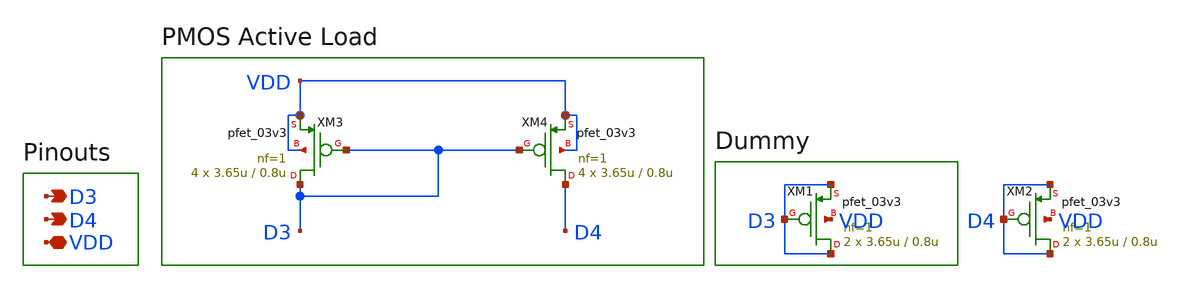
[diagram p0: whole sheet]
** sch_path: designs/libs/core_ota/active_load/active_load.sch
**.subckt active_load VDD D3 D4
*.iopin VDD
*.opin D3
*.opin D4
XM3 D3 D3 VDD VDD pfet_03v3 L=0.8u W=3.65u nf=1 ad='int((nf+1)/2) * W/nf * 0.18u' as='int((nf+2)/2) * W/nf * 0.18u'
+ pd='2*int((nf+1)/2) * (W/nf + 0.18u)' ps='2*int((nf+2)/2) * (W/nf + 0.18u)' nrd='0.18u / W' nrs='0.18u / W'
+ sa=0 sb=0 sd=0 m=4
XM4 D4 D3 VDD VDD pfet_03v3 L=0.8u W=3.65u nf=1 ad='int((nf+1)/2) * W/nf * 0.18u' as='int((nf+2)/2) * W/nf * 0.18u'
+ pd='2*int((nf+1)/2) * (W/nf + 0.18u)' ps='2*int((nf+2)/2) * (W/nf + 0.18u)' nrd='0.18u / W' nrs='0.18u / W'
+ sa=0 sb=0 sd=0 m=4
XM1 D3 D3 D3 VDD pfet_03v3 L=0.8u W=3.65u nf=1 ad='int((nf+1)/2) * W/nf * 0.18u' as='int((nf+2)/2) * W/nf * 0.18u'
+ pd='2*int((nf+1)/2) * (W/nf + 0.18u)' ps='2*int((nf+2)/2) * (W/nf + 0.18u)' nrd='0.18u / W' nrs='0.18u / W'
+ sa=0 sb=0 sd=0 m=2
XM2 D4 D4 D4 VDD pfet_03v3 L=0.8u W=3.65u nf=1 ad='int((nf+1)/2) * W/nf * 0.18u' as='int((nf+2)/2) * W/nf * 0.18u'
+ pd='2*int((nf+1)/2) * (W/nf + 0.18u)' ps='2*int((nf+2)/2) * (W/nf + 0.18u)' nrd='0.18u / W' nrs='0.18u / W'
+ sa=0 sb=0 sd=0 m=2
**.ends
.end
